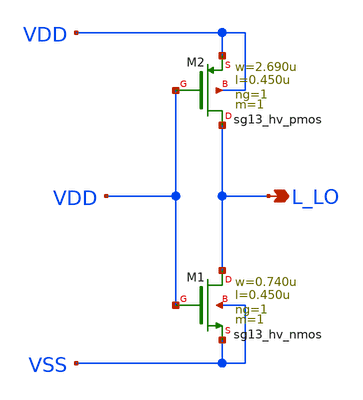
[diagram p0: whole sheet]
** sch_path: ihp-sg13g2/libs.ref/sg13g2_stdcell_hv/sch/xschem/sg13g2_hv_tielo.sch
* Copyright 2023 IHP PDK Authors
* Licensed under the Apache License, Version 2.0 (the "License");
* you may not use this file except in compliance with the License.
* You may obtain a copy of the License at
* https://www.apache.org/licenses/LICENSE-2.0
* Unless required by applicable law or agreed to in writing, software
* distributed under the License is distributed on an "AS IS" BASIS,
* WITHOUT WARRANTIES OR CONDITIONS OF ANY KIND, either express or implied.
* See the License for the specific language governing permissions and
* limitations under the License.
**.subckt sg13g2_hv_tielo L_LO
*.opin L_LO
XM1 L_LO VDD VSS VSS sg13_hv_nmos w=0.740u l=0.450u ng=1 m=1 mm_ok=1
XM2 L_LO VDD VDD VDD sg13_hv_pmos w=2.690u l=0.450u ng=1 m=1 mm_ok=1
**.ends
.end
